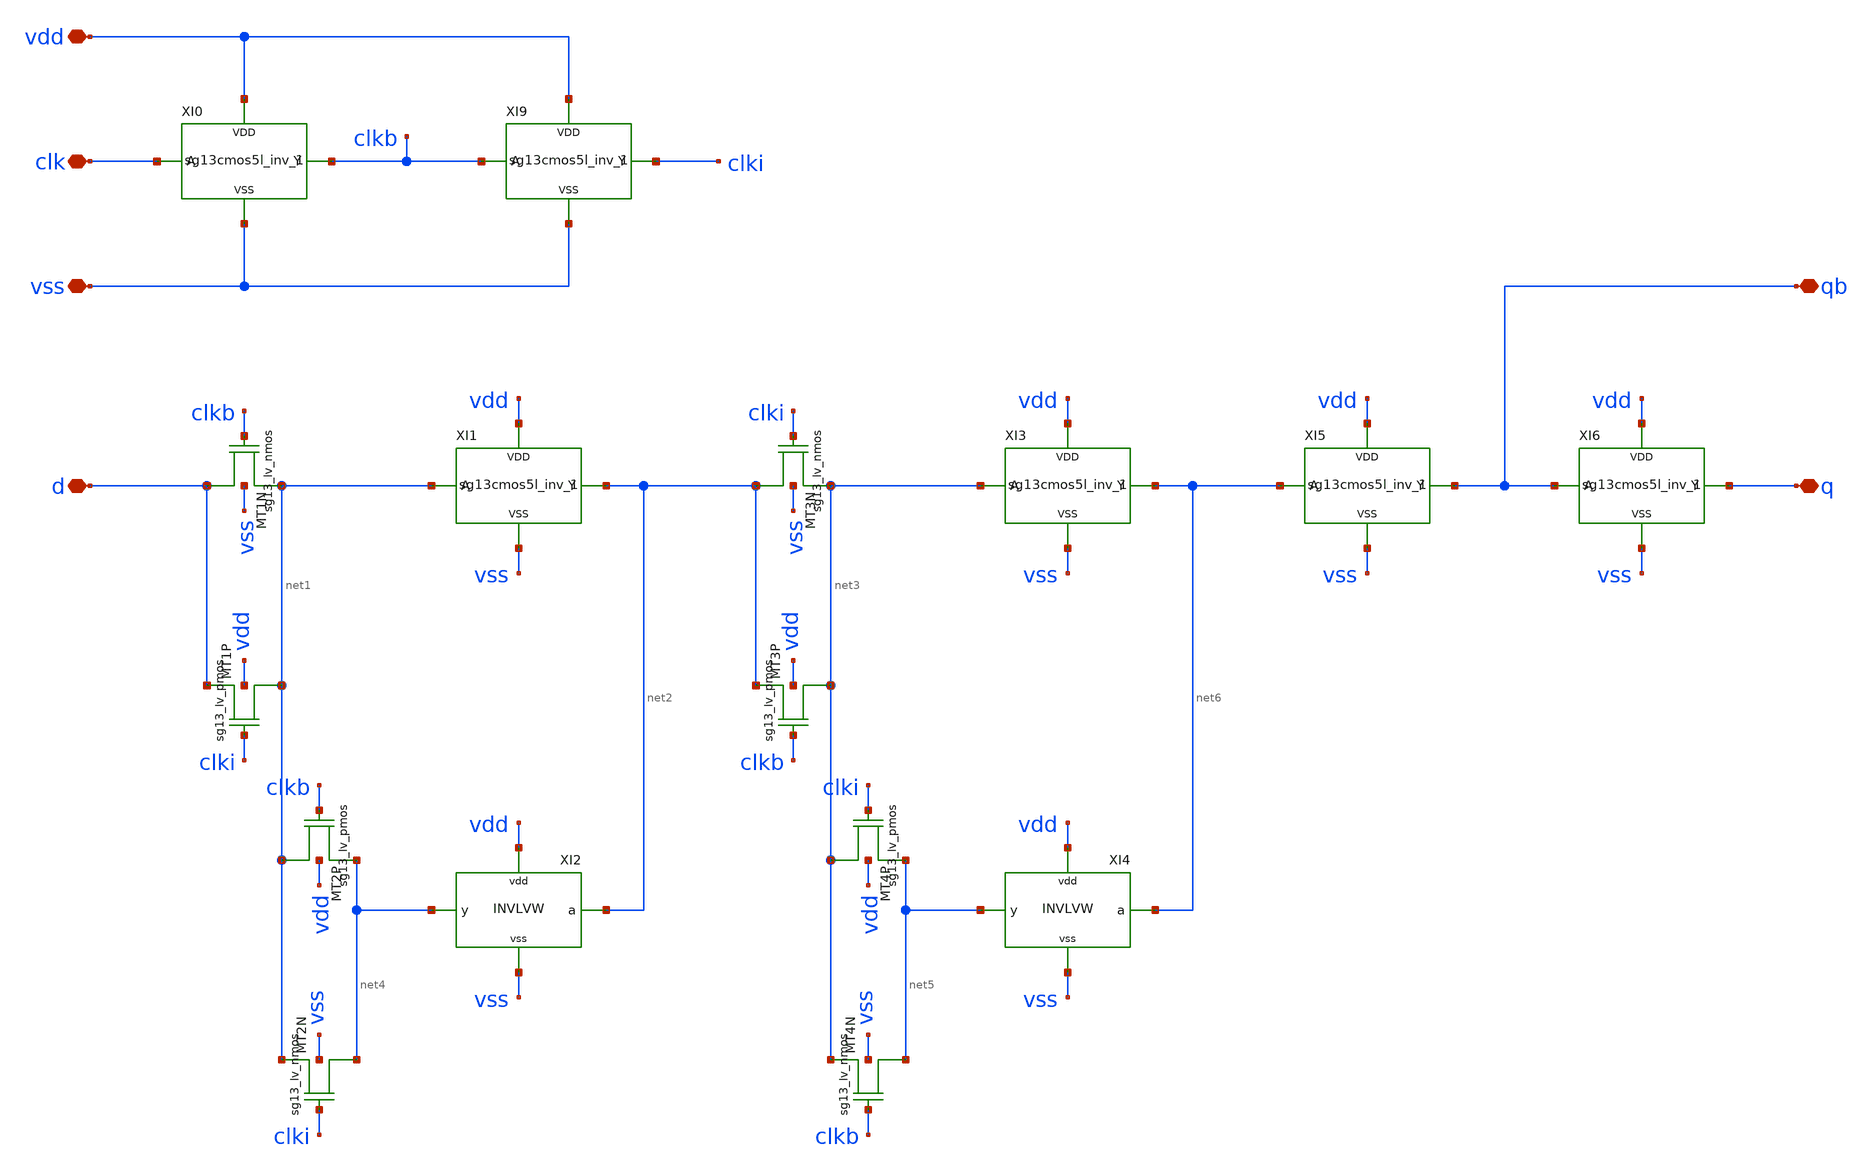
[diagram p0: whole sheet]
** sch_path: xschem/schematics/dff_c2mos.sch
**.subckt dff_c2mos d q qb clk vdd vss
*.iopin d
*.iopin q
*.iopin qb
*.iopin clk
*.iopin vdd
*.iopin vss
XMT1N net1 clkb d vss sg13_lv_nmos w=0.6u l=0.13u ng=1 m=1
XMT1P d clki net1 vdd sg13_lv_pmos w=1.2u l=0.13u ng=1 m=1
XMT3N net3 clki net2 vss sg13_lv_nmos w=0.6u l=0.13u ng=1 m=1
XMT3P net2 clkb net3 vdd sg13_lv_pmos w=1.2u l=0.13u ng=1 m=1
XMT2P net4 clkb net1 vdd sg13_lv_pmos w=0.6u l=0.13u ng=1 m=1
XMT2N net1 clki net4 vss sg13_lv_nmos w=0.3u l=0.13u ng=1 m=1
XMT4P net5 clki net3 vdd sg13_lv_pmos w=0.6u l=0.13u ng=1 m=1
XMT4N net3 clkb net5 vss sg13_lv_nmos w=0.3u l=0.13u ng=1 m=1
XI1 net2 net1 vdd vss sg13cmos5l_inv_1
XI3 net6 net3 vdd vss sg13cmos5l_inv_1
XI5 qb net6 vdd vss sg13cmos5l_inv_1
XI6 q qb vdd vss sg13cmos5l_inv_1
XI2 net2 net4 vdd vss INVLVW
XI4 net6 net5 vdd vss INVLVW
XI0 clkb clk vdd vss sg13cmos5l_inv_1
XI9 clki clkb vdd vss sg13cmos5l_inv_1
**.ends

* expanding   symbol:  logic_gates/sg13cmos5l_inv_1.sym # of pins=4
** sym_path: xschem/logic_gates/sg13cmos5l_inv_1.sym
** sch_path: xschem/logic_gates/sg13cmos5l_inv_1.sch
.subckt sg13cmos5l_inv_1 Y A VDD VSS
*.iopin Y
*.iopin A
*.iopin VDD
*.iopin VSS
XMN0 Y A VSS VSS sg13_lv_nmos w=0.74u l=0.13u ng=1 m=1
XMP0 VDD A Y VDD sg13_lv_pmos w=1.12u l=0.13u ng=1 m=1
.ends


* expanding   symbol:  logic_gates/INVLVW.sym # of pins=4
** sym_path: xschem/logic_gates/INVLVW.sym
** sch_path: xschem/logic_gates/INVLVW.sch
.subckt INVLVW a y vdd vss
*.iopin vdd
*.iopin vss
*.iopin y
*.iopin a
XMP vdd a y vdd sg13_lv_pmos w=0.3u l=0.3u ng=1 m=1
XMN y a vss vss sg13_lv_nmos w=0.3u l=0.3u ng=1 m=1
.ends

.end
